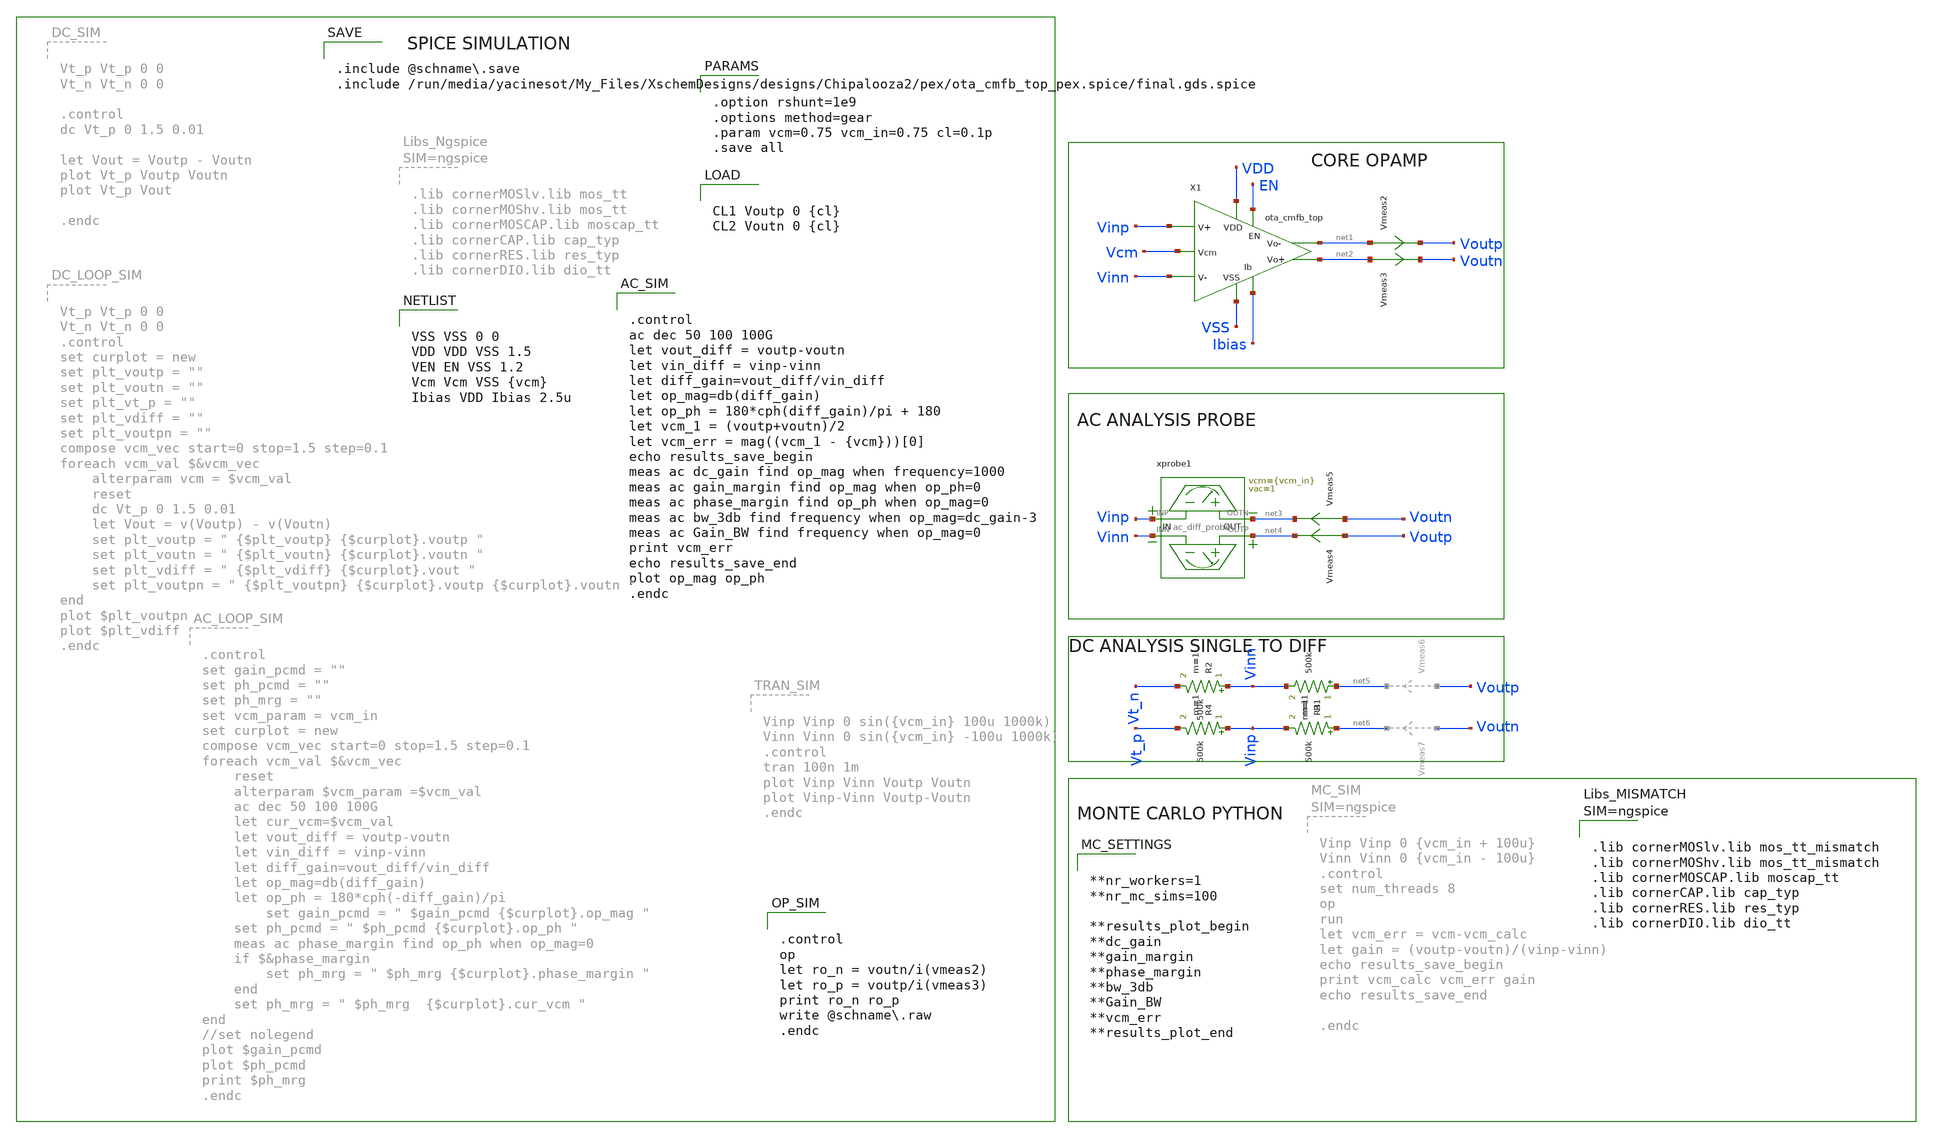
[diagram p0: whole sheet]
** sch_path: schema/ota_cmfb_top_pex_tb.sch
**.subckt ota_cmfb_top_pex_tb
xprobe1 Vinp net3 Vinn net4 ac_diff_probe vcm={vcm_in} vac=1
Vmeas2 net1 Voutp 0
.save i(vmeas2)
Vmeas3 net2 Voutn 0
.save i(vmeas3)
Vmeas4 Voutp net4 0
.save i(vmeas4)
Vmeas5 Voutn net3 0
.save i(vmeas5)
R1 net5 Vinn 500k m=1
R2 Vinn Vt_n 500k m=1
R3 net6 Vinp 500k m=1
R4 Vinp Vt_p 500k m=1
X1 VDD VSS EN Vinp Vinn Vcm Ibias net2 net1 ota_cmfb_top
**** begin user architecture code


VSS VSS 0 0
VDD VDD VSS 1.5
VEN EN VSS 1.2
Vcm Vcm VSS {vcm}
Ibias VDD Ibias 2.5u



.control
op
let ro_n = voutn/i(vmeas2)
let ro_p = voutp/i(vmeas3)
print ro_n ro_p
write @schname.raw
.endc



.control
ac dec 50 100 100G
let vout_diff = voutp-voutn
let vin_diff = vinp-vinn
let diff_gain=vout_diff/vin_diff
let op_mag=db(diff_gain)
let op_ph = 180*cph(diff_gain)/pi + 180
let vcm_1 = (voutp+voutn)/2
let vcm_err = mag((vcm_1 - {vcm}))[0]
echo results_save_begin
meas ac dc_gain find op_mag when frequency=1000
meas ac gain_margin find op_mag when op_ph=0
meas ac phase_margin find op_ph when op_mag=0
meas ac bw_3db find frequency when op_mag=dc_gain-3
meas ac Gain_BW find frequency when op_mag=0
print vcm_err
echo results_save_end
plot op_mag op_ph
.endc




.option rshunt=1e9
.options method=gear
.param vcm=0.75 vcm_in=0.75 cl=0.1p
.save all




CL1 Voutp 0 {cl}
CL2 Voutn 0 {cl}



.include @schname.save
.include /run/media/yacinesot/My_Files/XschemDesigns/designs/Chipalooza2/pex/ota_cmfb_top_pex.spice/final.gds.spice



**nr_workers=1
**nr_mc_sims=100

**results_plot_begin
**dc_gain
**gain_margin
**phase_margin
**bw_3db
**Gain_BW
**vcm_err
**results_plot_end





.lib cornerMOSlv.lib mos_tt_mismatch
.lib cornerMOShv.lib mos_tt_mismatch
.lib cornerMOSCAP.lib moscap_tt
.lib cornerCAP.lib cap_typ
.lib cornerRES.lib res_typ
.lib cornerDIO.lib dio_tt



**** end user architecture code
**.ends

* expanding   symbol:  ac_diff_probe/ac_diff_probe.sym # of pins=4
** sym_path: schema/ac_diff_probe/ac_diff_probe.sym
** sch_path: schema/ac_diff_probe/ac_diff_probe.sch
.subckt ac_diff_probe INP OUTN INN OUTP  vcm=0.75 vac=0.1
*.iopin OUTN
*.iopin INP
*.iopin OUTP
*.iopin INN
xprobe1 OUTN INP ac_probe vcm={vcm} vac={vac}
xprobe2 OUTP INN ac_probe vcm={vcm} vac=-{vac}
.ends


* expanding   symbol:  ac_probe/ac_probe.sym # of pins=2
** sym_path: schema/ac_probe/ac_probe.sym
** sch_path: schema/ac_probe/ac_probe.sch
.subckt ac_probe OUT IN  vcm=0.75 vac=0.01

*.iopin IN
*.iopin OUT
C1 0 IN 1 m=1
V1 IN 0 {vcm} ac {vac}
R1 OUT IN 1G m=1
.ends

.end
